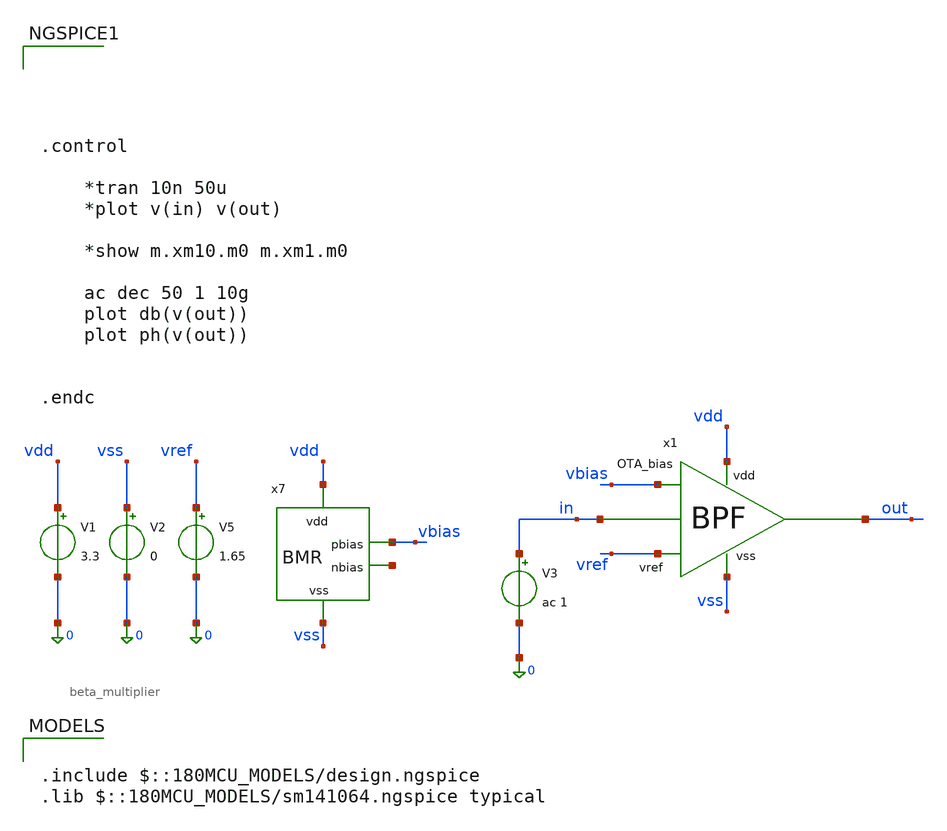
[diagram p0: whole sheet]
** sch_path: simulation/testbench_analog/BPF/BPF_freq-response.sch
**.subckt BPF_freq-response
x1 vdd in out vbias vref vss BPF
V3 in 0 ac 1
V1 vdd 0 3.3
V2 vss 0 0
V5 vref 0 1.65
x7 vdd vbias net1 vss beta_multiplier
**** begin user architecture code

.include $::180MCU_MODELS/design.ngspice
.lib $::180MCU_MODELS/sm141064.ngspice typical






.control

	*tran 10n 50u
	*plot v(in) v(out)

	*show m.xm10.m0 m.xm1.m0

	ac dec 50 1 10g
	plot db(v(out))
	plot ph(v(out))


.endc


**** end user architecture code
**.ends

* expanding   symbol:  BPF.sym # of pins=6
** sym_path: design/analog/BPF/BPF.sym
** sch_path: design/analog/BPF/BPF.sch
.subckt BPF vdd in out OTA_bias vref vss
*.opin out
*.ipin in
*.iopin vdd
*.iopin vss
*.iopin vref
*.ipin OTA_bias
R2 net2 in 30k m=1
C2 out net2 20p m=1
R3 net1 out 120k m=1
R7 vref net2 10k m=1
C7 net1 net2 20p m=1
x1 vdd out vref net1 OTA_bias vss two-stage_miller_OTA
.ends


* expanding   symbol:  acoustic-ranger-dvl-processor/design/analog/beta
*+ multiplier/beta_multiplier.sym # of pins=4
** sym_path: design/analog/beta multiplier/beta_multiplier.sym
** sch_path: design/analog/beta multiplier/beta_multiplier.sch
.subckt beta_multiplier vdd pbias nbias vss
*.iopin vdd
*.iopin vss
*.opin pbias
*.opin nbias
XM14 pbias nbias net1 net1 nfet_03v3 L=10u W=13.8u nf=1 ad='int((nf+1)/2) * W/nf * 0.18u' as='int((nf+2)/2) * W/nf * 0.18u'
+ pd='2*int((nf+1)/2) * (W/nf + 0.18u)' ps='2*int((nf+2)/2) * (W/nf + 0.18u)' nrd='0.18u / W' nrs='0.18u / W'
+ sa=0 sb=0 sd=0 m=1
XM15 nbias nbias vss vss nfet_03v3 L=10u W=5.71u nf=1 ad='int((nf+1)/2) * W/nf * 0.18u' as='int((nf+2)/2) * W/nf * 0.18u'
+ pd='2*int((nf+1)/2) * (W/nf + 0.18u)' ps='2*int((nf+2)/2) * (W/nf + 0.18u)' nrd='0.18u / W' nrs='0.18u / W'
+ sa=0 sb=0 sd=0 m=1
XM16 pbias pbias vdd vdd pfet_03v3 L=10u W=40u nf=1 ad='int((nf+1)/2) * W/nf * 0.18u' as='int((nf+2)/2) * W/nf * 0.18u'
+ pd='2*int((nf+1)/2) * (W/nf + 0.18u)' ps='2*int((nf+2)/2) * (W/nf + 0.18u)' nrd='0.18u / W' nrs='0.18u / W'
+ sa=0 sb=0 sd=0 m=1
XM17 nbias pbias vdd vdd pfet_03v3 L=10u W=40u nf=1 ad='int((nf+1)/2) * W/nf * 0.18u' as='int((nf+2)/2) * W/nf * 0.18u'
+ pd='2*int((nf+1)/2) * (W/nf + 0.18u)' ps='2*int((nf+2)/2) * (W/nf + 0.18u)' nrd='0.18u / W' nrs='0.18u / W'
+ sa=0 sb=0 sd=0 m=1
R3 net1 vss 9.012k m=1
.ends


* expanding   symbol:  acoustic_ranger_2026/two-stage_miller_OTA.sym # of pins=6
** sym_path: design/analog/OTA/two-stage_miller_OTA.sym
** sch_path: design/analog/OTA/two-stage_miller_OTA.sch
.subckt two-stage_miller_OTA vdd out in+ in- bias vss
*.ipin in+
*.ipin in-
*.opin out
*.iopin vdd
*.iopin vss
*.ipin bias
XM1 net2 in- net1 vdd pfet_03v3 L=1u W=6.2u nf=1 ad='int((nf+1)/2) * W/nf * 0.18u' as='int((nf+2)/2) * W/nf * 0.18u'
+ pd='2*int((nf+1)/2) * (W/nf + 0.18u)' ps='2*int((nf+2)/2) * (W/nf + 0.18u)' nrd='0.18u / W' nrs='0.18u / W'
+ sa=0 sb=0 sd=0 m=8
XM2 net3 in+ net1 vdd pfet_03v3 L=1u W=6.2u nf=1 ad='int((nf+1)/2) * W/nf * 0.18u' as='int((nf+2)/2) * W/nf * 0.18u'
+ pd='2*int((nf+1)/2) * (W/nf + 0.18u)' ps='2*int((nf+2)/2) * (W/nf + 0.18u)' nrd='0.18u / W' nrs='0.18u / W'
+ sa=0 sb=0 sd=0 m=8
XM14 net3 net2 vss vss nfet_03v3 L=3u W=7.7u nf=4 ad='int((nf+1)/2) * W/nf * 0.18u' as='int((nf+2)/2) * W/nf * 0.18u'
+ pd='2*int((nf+1)/2) * (W/nf + 0.18u)' ps='2*int((nf+2)/2) * (W/nf + 0.18u)' nrd='0.18u / W' nrs='0.18u / W'
+ sa=0 sb=0 sd=0 m=2
XM15 net2 net2 vss vss nfet_03v3 L=3u W=7.7u nf=4 ad='int((nf+1)/2) * W/nf * 0.18u' as='int((nf+2)/2) * W/nf * 0.18u'
+ pd='2*int((nf+1)/2) * (W/nf + 0.18u)' ps='2*int((nf+2)/2) * (W/nf + 0.18u)' nrd='0.18u / W' nrs='0.18u / W'
+ sa=0 sb=0 sd=0 m=2
XM3 out net3 vss vss nfet_03v3 L=3u W=7.7u nf=4 ad='int((nf+1)/2) * W/nf * 0.18u' as='int((nf+2)/2) * W/nf * 0.18u'
+ pd='2*int((nf+1)/2) * (W/nf + 0.18u)' ps='2*int((nf+2)/2) * (W/nf + 0.18u)' nrd='0.18u / W' nrs='0.18u / W'
+ sa=0 sb=0 sd=0 m=12
C1 out net3 5p m=1
XM4 net1 bias vdd vdd pfet_03v3 L=20u W=25.3u nf=2 ad='int((nf+1)/2) * W/nf * 0.18u' as='int((nf+2)/2) * W/nf * 0.18u'
+ pd='2*int((nf+1)/2) * (W/nf + 0.18u)' ps='2*int((nf+2)/2) * (W/nf + 0.18u)' nrd='0.18u / W' nrs='0.18u / W'
+ sa=0 sb=0 sd=0 m=2
XM5 out bias vdd vdd pfet_03v3 L=20u W=25.3u nf=2 ad='int((nf+1)/2) * W/nf * 0.18u' as='int((nf+2)/2) * W/nf * 0.18u'
+ pd='2*int((nf+1)/2) * (W/nf + 0.18u)' ps='2*int((nf+2)/2) * (W/nf + 0.18u)' nrd='0.18u / W' nrs='0.18u / W'
+ sa=0 sb=0 sd=0 m=6
.ends

.end
